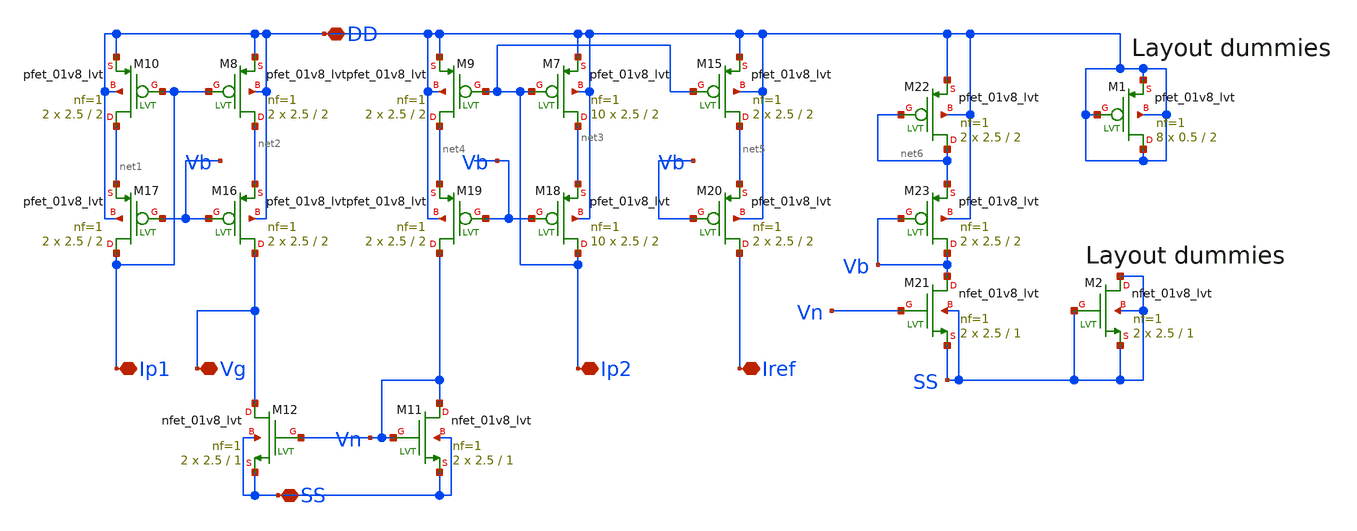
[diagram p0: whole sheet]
** sch_path: xschem/iref_2nA_mirrors.sch
**.subckt iref_2nA_mirrors DD SS Iref Ip2 Vg Ip1
*.iopin DD
*.iopin SS
*.iopin Iref
*.iopin Ip2
*.iopin Vg
*.iopin Ip1
XM7 net3 Ip2 DD DD sky130_fd_pr__pfet_01v8_lvt L=2 W=2.5 nf=1 ad='int((nf+1)/2) * W/nf * 0.29' as='int((nf+2)/2) * W/nf * 0.29'
+ pd='2*int((nf+1)/2) * (W/nf + 0.29)' ps='2*int((nf+2)/2) * (W/nf + 0.29)' nrd='0.29 / W' nrs='0.29 / W'
+ sa=0 sb=0 sd=0 mult=10 m=10
XM8 net2 Ip1 DD DD sky130_fd_pr__pfet_01v8_lvt L=2 W=2.5 nf=1 ad='int((nf+1)/2) * W/nf * 0.29' as='int((nf+2)/2) * W/nf * 0.29'
+ pd='2*int((nf+1)/2) * (W/nf + 0.29)' ps='2*int((nf+2)/2) * (W/nf + 0.29)' nrd='0.29 / W' nrs='0.29 / W'
+ sa=0 sb=0 sd=0 mult=2 m=2
XM9 net4 Ip2 DD DD sky130_fd_pr__pfet_01v8_lvt L=2 W=2.5 nf=1 ad='int((nf+1)/2) * W/nf * 0.29' as='int((nf+2)/2) * W/nf * 0.29'
+ pd='2*int((nf+1)/2) * (W/nf + 0.29)' ps='2*int((nf+2)/2) * (W/nf + 0.29)' nrd='0.29 / W' nrs='0.29 / W'
+ sa=0 sb=0 sd=0 mult=2 m=2
XM10 net1 Ip1 DD DD sky130_fd_pr__pfet_01v8_lvt L=2 W=2.5 nf=1 ad='int((nf+1)/2) * W/nf * 0.29' as='int((nf+2)/2) * W/nf * 0.29'
+ pd='2*int((nf+1)/2) * (W/nf + 0.29)' ps='2*int((nf+2)/2) * (W/nf + 0.29)' nrd='0.29 / W' nrs='0.29 / W'
+ sa=0 sb=0 sd=0 mult=2 m=2
XM11 Vn Vn SS SS sky130_fd_pr__nfet_01v8_lvt L=1 W=2.5 nf=1 ad='int((nf+1)/2) * W/nf * 0.29' as='int((nf+2)/2) * W/nf * 0.29'
+ pd='2*int((nf+1)/2) * (W/nf + 0.29)' ps='2*int((nf+2)/2) * (W/nf + 0.29)' nrd='0.29 / W' nrs='0.29 / W'
+ sa=0 sb=0 sd=0 mult=2 m=2
XM12 Vg Vn SS SS sky130_fd_pr__nfet_01v8_lvt L=1 W=2.5 nf=1 ad='int((nf+1)/2) * W/nf * 0.29' as='int((nf+2)/2) * W/nf * 0.29'
+ pd='2*int((nf+1)/2) * (W/nf + 0.29)' ps='2*int((nf+2)/2) * (W/nf + 0.29)' nrd='0.29 / W' nrs='0.29 / W'
+ sa=0 sb=0 sd=0 mult=2 m=2
XM15 net5 Ip2 DD DD sky130_fd_pr__pfet_01v8_lvt L=2 W=2.5 nf=1 ad='int((nf+1)/2) * W/nf * 0.29' as='int((nf+2)/2) * W/nf * 0.29'
+ pd='2*int((nf+1)/2) * (W/nf + 0.29)' ps='2*int((nf+2)/2) * (W/nf + 0.29)' nrd='0.29 / W' nrs='0.29 / W'
+ sa=0 sb=0 sd=0 mult=2 m=2
XM16 Vg Vb net2 DD sky130_fd_pr__pfet_01v8_lvt L=2 W=2.5 nf=1 ad='int((nf+1)/2) * W/nf * 0.29' as='int((nf+2)/2) * W/nf * 0.29'
+ pd='2*int((nf+1)/2) * (W/nf + 0.29)' ps='2*int((nf+2)/2) * (W/nf + 0.29)' nrd='0.29 / W' nrs='0.29 / W'
+ sa=0 sb=0 sd=0 mult=2 m=2
XM17 Ip1 Vb net1 DD sky130_fd_pr__pfet_01v8_lvt L=2 W=2.5 nf=1 ad='int((nf+1)/2) * W/nf * 0.29' as='int((nf+2)/2) * W/nf * 0.29'
+ pd='2*int((nf+1)/2) * (W/nf + 0.29)' ps='2*int((nf+2)/2) * (W/nf + 0.29)' nrd='0.29 / W' nrs='0.29 / W'
+ sa=0 sb=0 sd=0 mult=2 m=2
XM18 Ip2 Vb net3 DD sky130_fd_pr__pfet_01v8_lvt L=2 W=2.5 nf=1 ad='int((nf+1)/2) * W/nf * 0.29' as='int((nf+2)/2) * W/nf * 0.29'
+ pd='2*int((nf+1)/2) * (W/nf + 0.29)' ps='2*int((nf+2)/2) * (W/nf + 0.29)' nrd='0.29 / W' nrs='0.29 / W'
+ sa=0 sb=0 sd=0 mult=10 m=10
XM19 Vn Vb net4 DD sky130_fd_pr__pfet_01v8_lvt L=2 W=2.5 nf=1 ad='int((nf+1)/2) * W/nf * 0.29' as='int((nf+2)/2) * W/nf * 0.29'
+ pd='2*int((nf+1)/2) * (W/nf + 0.29)' ps='2*int((nf+2)/2) * (W/nf + 0.29)' nrd='0.29 / W' nrs='0.29 / W'
+ sa=0 sb=0 sd=0 mult=2 m=2
XM20 Iref Vb net5 DD sky130_fd_pr__pfet_01v8_lvt L=2 W=2.5 nf=1 ad='int((nf+1)/2) * W/nf * 0.29' as='int((nf+2)/2) * W/nf * 0.29'
+ pd='2*int((nf+1)/2) * (W/nf + 0.29)' ps='2*int((nf+2)/2) * (W/nf + 0.29)' nrd='0.29 / W' nrs='0.29 / W'
+ sa=0 sb=0 sd=0 mult=2 m=2
XM22 net6 net6 DD DD sky130_fd_pr__pfet_01v8_lvt L=2 W=2.5 nf=1 ad='int((nf+1)/2) * W/nf * 0.29' as='int((nf+2)/2) * W/nf * 0.29'
+ pd='2*int((nf+1)/2) * (W/nf + 0.29)' ps='2*int((nf+2)/2) * (W/nf + 0.29)' nrd='0.29 / W' nrs='0.29 / W'
+ sa=0 sb=0 sd=0 mult=2 m=2
XM21 Vb Vn SS SS sky130_fd_pr__nfet_01v8_lvt L=1 W=2.5 nf=1 ad='int((nf+1)/2) * W/nf * 0.29' as='int((nf+2)/2) * W/nf * 0.29'
+ pd='2*int((nf+1)/2) * (W/nf + 0.29)' ps='2*int((nf+2)/2) * (W/nf + 0.29)' nrd='0.29 / W' nrs='0.29 / W'
+ sa=0 sb=0 sd=0 mult=2 m=2
XM23 Vb Vb net6 DD sky130_fd_pr__pfet_01v8_lvt L=2 W=2.5 nf=1 ad='int((nf+1)/2) * W/nf * 0.29' as='int((nf+2)/2) * W/nf * 0.29'
+ pd='2*int((nf+1)/2) * (W/nf + 0.29)' ps='2*int((nf+2)/2) * (W/nf + 0.29)' nrd='0.29 / W' nrs='0.29 / W'
+ sa=0 sb=0 sd=0 mult=2 m=2
XM1 DD DD DD DD sky130_fd_pr__pfet_01v8_lvt L=2 W=0.5 nf=1 ad='int((nf+1)/2) * W/nf * 0.29' as='int((nf+2)/2) * W/nf * 0.29'
+ pd='2*int((nf+1)/2) * (W/nf + 0.29)' ps='2*int((nf+2)/2) * (W/nf + 0.29)' nrd='0.29 / W' nrs='0.29 / W'
+ sa=0 sb=0 sd=0 mult=8 m=8
XM2 SS SS SS SS sky130_fd_pr__nfet_01v8_lvt L=1 W=2.5 nf=1 ad='int((nf+1)/2) * W/nf * 0.29' as='int((nf+2)/2) * W/nf * 0.29'
+ pd='2*int((nf+1)/2) * (W/nf + 0.29)' ps='2*int((nf+2)/2) * (W/nf + 0.29)' nrd='0.29 / W' nrs='0.29 / W'
+ sa=0 sb=0 sd=0 mult=2 m=2
**.ends
.end
